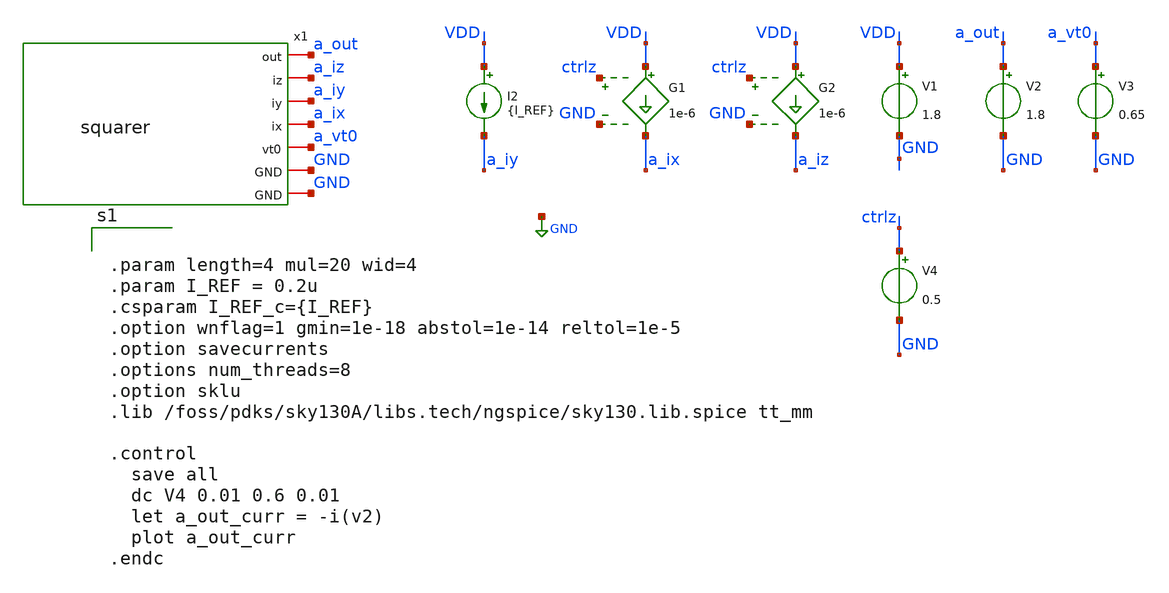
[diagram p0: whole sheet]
** sch_path: xschem/archive/old_blocks/squarer_tb.sch
**.subckt squarer_tb
I2 VDD a_iy {I_REF}
G1 VDD a_ix ctrlz GND 1e-6
G2 VDD a_iz ctrlz GND 1e-6
V1 VDD GND 1.8
V2 a_out GND 1.8
V3 a_vt0 GND 0.65
V4 ctrlz GND 0.5
x1 a_out a_iz a_iy a_ix a_vt0 GND squarer
**** begin user architecture code


.param length=4 mul=20 wid=4
.param I_REF = 0.2u
.csparam I_REF_c={I_REF}
.option wnflag=1 gmin=1e-18 abstol=1e-14 reltol=1e-5
.option savecurrents
.options num_threads=8
.option sklu
.lib /foss/pdks/sky130A/libs.tech/ngspice/sky130.lib.spice tt_mm

.control
  save all
  dc V4 0.01 0.6 0.01
  let a_out_curr = -i(v2)
  plot a_out_curr
.endc


**** end user architecture code
**.ends

* expanding   symbol:  archive/old_blocks/squarer.sym # of pins=7
** sym_path: xschem/archive/old_blocks/squarer.sym
** sch_path: xschem/archive/old_blocks/squarer.sch
.subckt squarer out iz iy ix vt0 GND
*.iopin vt0
*.iopin ix
*.iopin iy
*.iopin iz
*.iopin out
*.iopin GND
*.iopin GND
XM18 net1 ix GND GND sky130_fd_pr__nfet_01v8 L=4 W=1.2 nf=1 ad='int((nf+1)/2) * W/nf * 0.29' as='int((nf+2)/2) * W/nf * 0.29'
+ pd='2*int((nf+1)/2) * (W/nf + 0.29)' ps='2*int((nf+2)/2) * (W/nf + 0.29)' nrd='0.29 / W' nrs='0.29 / W'
+ sa=0 sb=0 sd=0 mult=1 m=1
XM1 ix vt0 net1 GND sky130_fd_pr__nfet_01v8 L=length W=wid nf=1 ad='int((nf+1)/2) * W/nf * 0.29' as='int((nf+2)/2) * W/nf * 0.29'
+ pd='2*int((nf+1)/2) * (W/nf + 0.29)' ps='2*int((nf+2)/2) * (W/nf + 0.29)' nrd='0.29 / W' nrs='0.29 / W'
+ sa=0 sb=0 sd=0 mult=mul m=mul
XM2 net2 iz GND GND sky130_fd_pr__nfet_01v8 L=4 W=1.2 nf=1 ad='int((nf+1)/2) * W/nf * 0.29' as='int((nf+2)/2) * W/nf * 0.29'
+ pd='2*int((nf+1)/2) * (W/nf + 0.29)' ps='2*int((nf+2)/2) * (W/nf + 0.29)' nrd='0.29 / W' nrs='0.29 / W'
+ sa=0 sb=0 sd=0 mult=1 m=1
XM3 iz iy net2 GND sky130_fd_pr__nfet_01v8 L=length W=wid nf=1 ad='int((nf+1)/2) * W/nf * 0.29' as='int((nf+2)/2) * W/nf * 0.29'
+ pd='2*int((nf+1)/2) * (W/nf + 0.29)' ps='2*int((nf+2)/2) * (W/nf + 0.29)' nrd='0.29 / W' nrs='0.29 / W'
+ sa=0 sb=0 sd=0 mult=mul m=mul
XM4 iy iy net1 GND sky130_fd_pr__nfet_01v8 L=length W=wid nf=1 ad='int((nf+1)/2) * W/nf * 0.29' as='int((nf+2)/2) * W/nf * 0.29'
+ pd='2*int((nf+1)/2) * (W/nf + 0.29)' ps='2*int((nf+2)/2) * (W/nf + 0.29)' nrd='0.29 / W' nrs='0.29 / W'
+ sa=0 sb=0 sd=0 mult=mul m=mul
XM5 net3 vt0 net2 GND sky130_fd_pr__nfet_01v8 L=length W=wid nf=1 ad='int((nf+1)/2) * W/nf * 0.29' as='int((nf+2)/2) * W/nf * 0.29'
+ pd='2*int((nf+1)/2) * (W/nf + 0.29)' ps='2*int((nf+2)/2) * (W/nf + 0.29)' nrd='0.29 / W' nrs='0.29 / W'
+ sa=0 sb=0 sd=0 mult=mul m=mul
XM26 net3 net3 out VDD sky130_fd_pr__pfet_01v8 L=length W=wid/2 nf=1 ad='int((1 + 1)/2) * wid/2 / 1 * 0.29'
+ as='int((1 + 2)/2) * wid/2 / 1 * 0.29' pd='2*int((1 + 1)/2) * (wid/2 / 1 + 0.29)' ps='2*int((1 + 2)/2) * (wid/2 / 1 + 0.29)'
+ nrd='0.29 / wid/2 ' nrs='0.29 / wid/2 ' sa=0 sb=0 sd=0 mult=mul m=mul
.ends

.GLOBAL GND
.end
